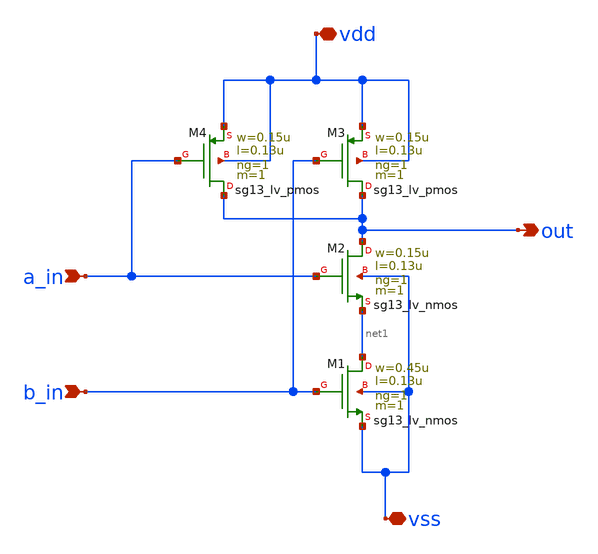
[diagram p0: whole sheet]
** sch_path: design/blocks/andgate/schematic/nand.sch
**.subckt nand vdd vss a_in b_in out
*.iopin vdd
*.iopin vss
*.ipin a_in
*.ipin b_in
*.opin out
XM1 net1 b_in vss vss sg13_lv_nmos w=0.45u l=0.13u ng=1 m=1 mm_ok=1
XM2 out a_in net1 vss sg13_lv_nmos w=0.15u l=0.13u ng=1 m=1 mm_ok=1
XM3 out b_in vdd vdd sg13_lv_pmos w=0.15u l=0.13u ng=1 m=1 mm_ok=1
XM4 out a_in vdd vdd sg13_lv_pmos w=0.15u l=0.13u ng=1 m=1 mm_ok=1
**.ends
.end
